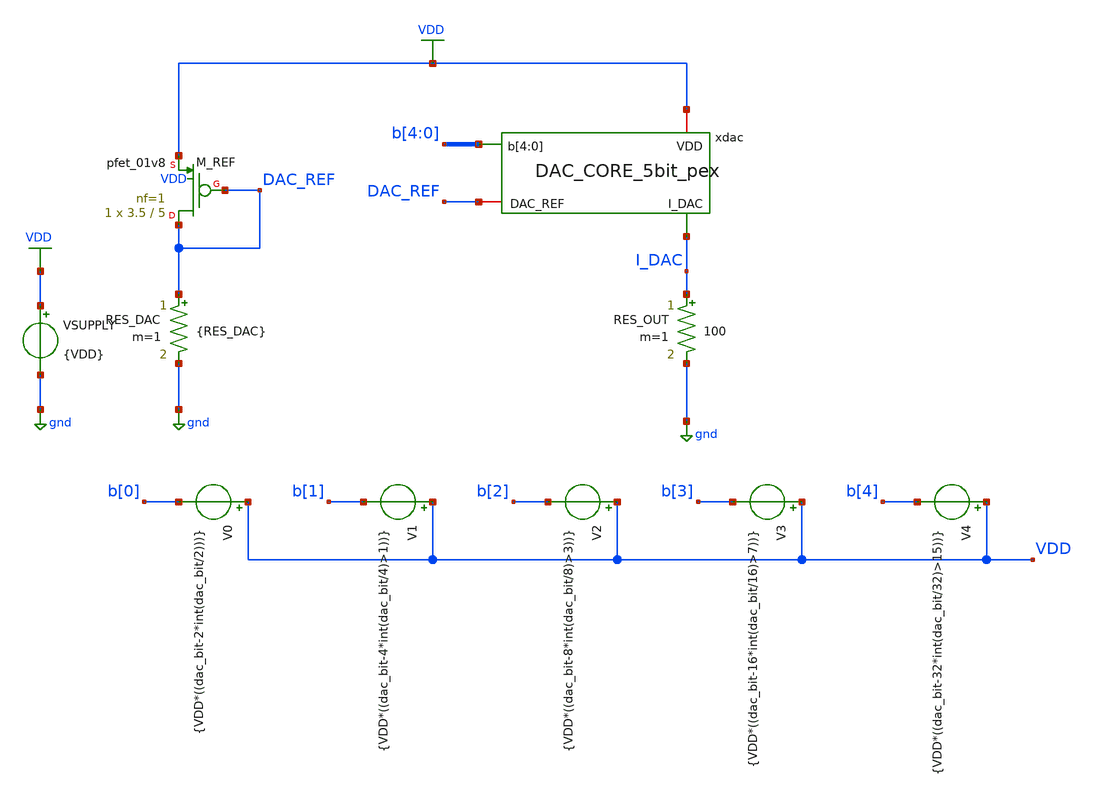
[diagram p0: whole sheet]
** sch_path: designs_backup/designs/lab2/xschem/DAC_CORE_5bit_test_pex.sch
**.subckt DAC_CORE_5bit_test_pex
RES_DAC DAC_REF gnd {RES_DAC} m=1
RES_OUT I_DAC gnd 100 m=1
V0 VDD b[0] {VDD*((dac_bit-2*int(dac_bit/2)))}
VSUPPLY VDD gnd {VDD}
V1 VDD b[1] {VDD*((dac_bit-4*int(dac_bit/4)>1))}
V2 VDD b[2] {VDD*((dac_bit-8*int(dac_bit/8)>3))}
V3 VDD b[3] {VDD*((dac_bit-16*int(dac_bit/16)>7))}
V4 VDD b[4] {VDD*((dac_bit-32*int(dac_bit/32)>15))}
XM_REF DAC_REF DAC_REF VDD VDD sky130_fd_pr__pfet_01v8 L=5 W=3.5 nf=1 ad='int((1 + 1)/2) * 3.5 / 1 * 0.29'
+ as='int((1 + 2)/2) * 3.5 / 1 * 0.29' pd='2*int((1 + 1)/2) * (3.5 / 1 + 0.29)' ps='2*int((1 + 2)/2) * (3.5 / 1 + 0.29)'
+ nrd='0.29 / 3.5 ' nrs='0.29 / 3.5 ' sa=0 sb=0 sd=0 mult=1 m=1
xdac VDD DAC_REF I_DAC b[4] b[3] b[2] b[1] b[0] DAC_CORE_5bit_pex
**** begin user architecture code


.options rshunt=1e12
.options gmin=1e-12
.options abstol=1e-10
.options rtol=1e-3

.param VDD = 1.8
.param RES_DAC = 11.37k
.param dac_bit = 0
.options savecurrents

.control
  shell mkdir -p /foss/designs/lab2/results/3.14
  shell rm -f /foss/designs/lab2/results/3.14/Idac_results.dat

  let d_val = 0
  reset
  op
  let Id_ref = @m.xm_ref.msky130_fd_pr__pfet_01v8[id] * 1e6
  let vth_ref = @m.xm_ref.msky130_fd_pr__pfet_01v8[vth]
  let vgs_ref = @m.xm_ref.msky130_fd_pr__pfet_01v8[vgs]
  echo -- Id_M_REF[uA]= $&Id_ref  | Vth_M_REF[V]= $&vth_ref | Vgs_M_REF[V]= $&vgs_ref -- >>
+ /foss/designs/lab2/results/3.14/Idac_results.dat
  echo >> /foss/designs/lab2/results/3.14/Idac_results.dat
  dowhile d_val <= 31
    alterparam dac_bit = $&d_val
    reset
    op
    let I_dac = @res_out[i] * 1e6
    echo dac_bit= $&d_val  |  I_dac[uA]= $&I_dac >> /foss/designs/lab2/results/3.14/Idac_results.dat
    let d_val = $&d_val + 1
  end
.endc



** opencircuitdesign pdks install
.lib $::SKYWATER_MODELS/sky130.lib.spice tt

* include pex spice netlist
.include /foss/designs/lab2/klayout/DAC_CORE_5bit_pex.spice

* force include MC files
.include "$::SKYWATER_MODELS/parameters/montecarlo.spice"
.include "$::SKYWATER_MODELS/parameters/critical.spice"

* force mismatch/process params
.param mc_mm_switch = 0
.param mc_pr_switch = 0

* disable pfet_ideal from mismatch/process
.subckt sky130_fd_pr__pfet_ideal D G S B W=0.42 L=0.15  nf=1 ad='int((1 + 1)/2) * {W} / 1 * 0.29' as='int((1 + 2)/2) * {W} / 1 * 0.29'
+  pd='2*int((1 + 1)/2) * ({W} / 1 + 0.29)' ps='2*int((1 + 2)/2) * ({W} / 1 + 0.29)'   nrd='0.29 / {W}'
+ nrs='0.29 / {W}' sa=0 sb=0 sd=0 mult=1
  .param mc_mm_switch=0
  .param mc_pr_switch=0
  XIDEAL D G S B sky130_fd_pr__pfet_01v8 W={W} L={L}
  + nf={nf} ad={ad} as={as} pd={pd} ps={ps}
  + nrd={nrd} nrs={nrs} sa={sa} sb={sb} sd={sd} mult={mult}
.ends

**** end user architecture code
**.ends
.GLOBAL gnd
.GLOBAL VDD
.end
